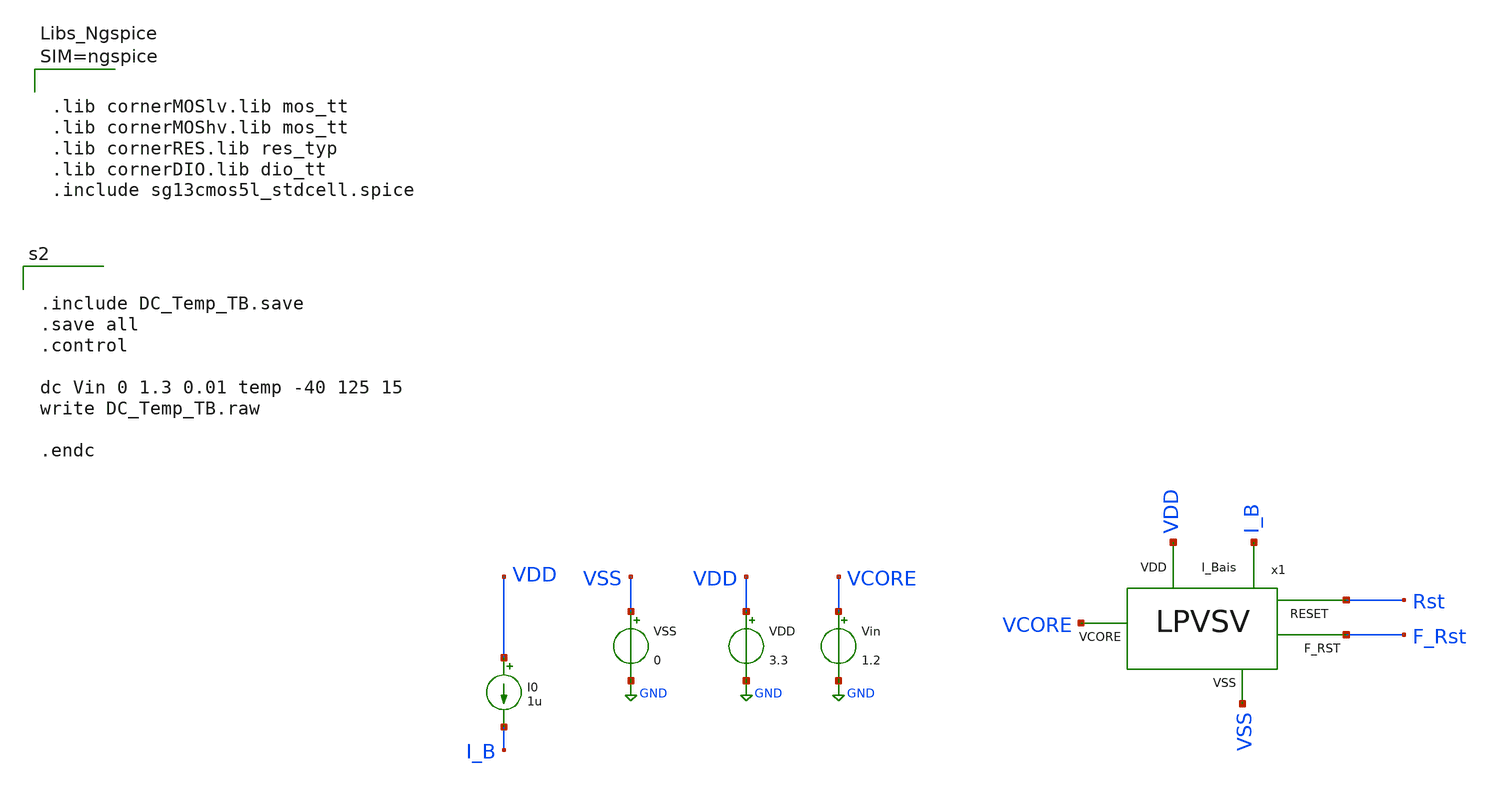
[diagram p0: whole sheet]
** sch_path: Simulation/DC_Analysis/DC_Temp_TB.sch
**.subckt DC_Temp_TB
VDD VDD GND 3.3
VSS VSS GND 0
Vin VCORE GND 1.2
I0 VDD I_B 1u
x1 VDD VCORE I_B Rst F_Rst VSS LPVSV
**** begin user architecture code


.include DC_Temp_TB.save
.save all
.control

dc Vin 0 1.3 0.01 temp -40 125 15
write DC_Temp_TB.raw

.endc




.options rshunt = 1e15
.options gmin=1e-9
.options reltol = 0.01 abstol = 1p
.option filetype=ascii





.lib cornerMOSlv.lib mos_tt
.lib cornerMOShv.lib mos_tt
.lib cornerRES.lib res_typ
.lib cornerDIO.lib dio_tt
.include sg13cmos5l_stdcell.spice



**** end user architecture code
**.ends
.GLOBAL GND
.end
